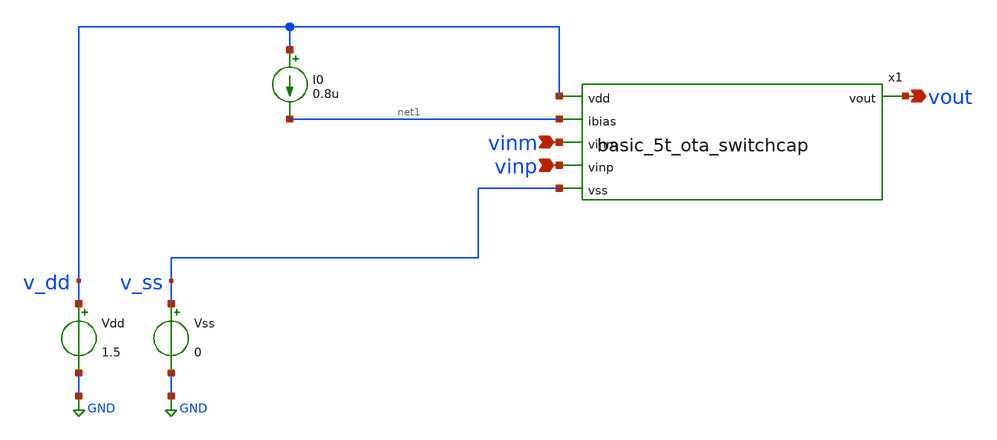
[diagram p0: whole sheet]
** sch_path: design/design_switch_cap/SC_ota_VCCS.sch
**.subckt SC_ota_VCCS vinm vinp vout
*.ipin vinm
*.ipin vinp
*.opin vout
Vss v_ss GND 0
I0 v_dd net1 0.8u
Vdd v_dd GND 1.5
x1 v_dd vout net1 vinm vinp v_ss basic_5t_ota_switchcap
**.ends

* expanding   symbol:  /foss/designs/analog-circuit-design/priyanka/basic_5t_ota_switchcap.sym # of
*+ pins=6
** sym_path: zip_meiners/ic_design/design_switch_cap/basic_5t_ota_switchcap.sym
** sch_path: zip_meiners/ic_design/design_switch_cap/basic_5t_ota_switchcap.sch
.subckt basic_5t_ota_switchcap vdd vout ibias vinm vinp vss
*.ipin vss
*.ipin vdd
*.ipin ibias
*.ipin vinm
*.ipin vinp
*.opin vout
XM1 vout net1 vdd vdd sg13_lv_pmos w=0.16u l=0.5u ng=1 m=1 mm_ok=1
XM2 vout vinm net2 vss sg13_lv_nmos w=0.15u l=2u ng=1 m=1 mm_ok=1
XM3 net1 net1 vdd vdd sg13_lv_pmos w=0.16u l=0.5u ng=1 m=1 mm_ok=1
XM4 net1 vinp net2 vss sg13_lv_nmos w=0.15u l=2u ng=1 m=1 mm_ok=1
XM5 net2 net3 vss vss sg13_lv_nmos w=0.3u l=2u ng=1 m=1 mm_ok=1
XM6 net4 net3 vss vss sg13_lv_nmos w=0.15u l=2u ng=1 m=1 mm_ok=1
XM7 net3 net3 vss vss sg13_lv_nmos w=0.15u l=2u ng=1 m=1 mm_ok=1
XM9 vdd ibias net4 vss sg13_lv_nmos w=0.15u l=2u ng=1 m=1 mm_ok=1
XM8 ibias ibias net3 vss sg13_lv_nmos w=0.15u l=2u ng=1 m=1 mm_ok=1
.ends

.GLOBAL GND
.end
